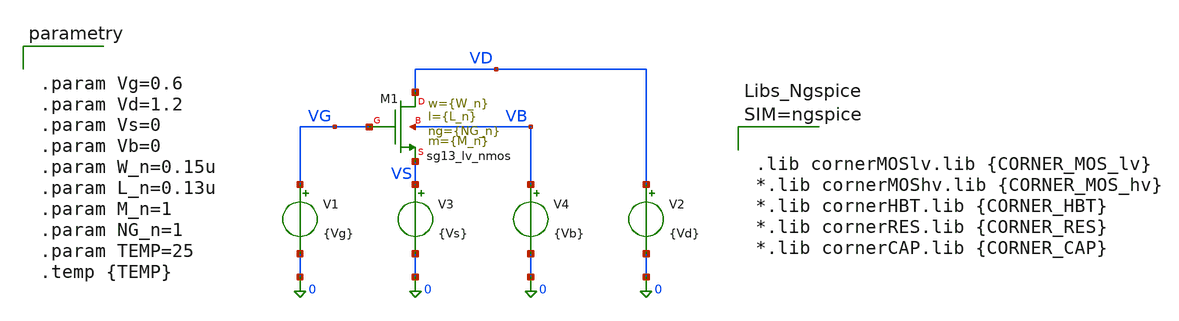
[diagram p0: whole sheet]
** sch_path: NMOS_lv_char/schematics/NMOS_lv_char.sch
**.subckt NMOS_lv_char
XM1 VD VG VS VB sg13_lv_nmos w={W_n} l={L_n} ng={NG_n} m={M_n} mm_ok=1
V1 VG 0 {Vg}
V2 VD 0 {Vd}
V3 VS 0 {Vs}
V4 VB 0 {Vb}
**** begin user architecture code



.lib cornerMOSlv.lib {CORNER_MOS_lv}
*.lib cornerMOShv.lib {CORNER_MOS_hv}
*.lib cornerHBT.lib {CORNER_HBT}
*.lib cornerRES.lib {CORNER_RES}
*.lib cornerCAP.lib {CORNER_CAP}





.param Vg=0.6
.param Vd=1.2
.param Vs=0
.param Vb=0
.param W_n=0.15u
.param L_n=0.13u
.param M_n=1
.param NG_n=1
.param TEMP=25
.temp {TEMP}


**** end user architecture code
**.ends
.end
